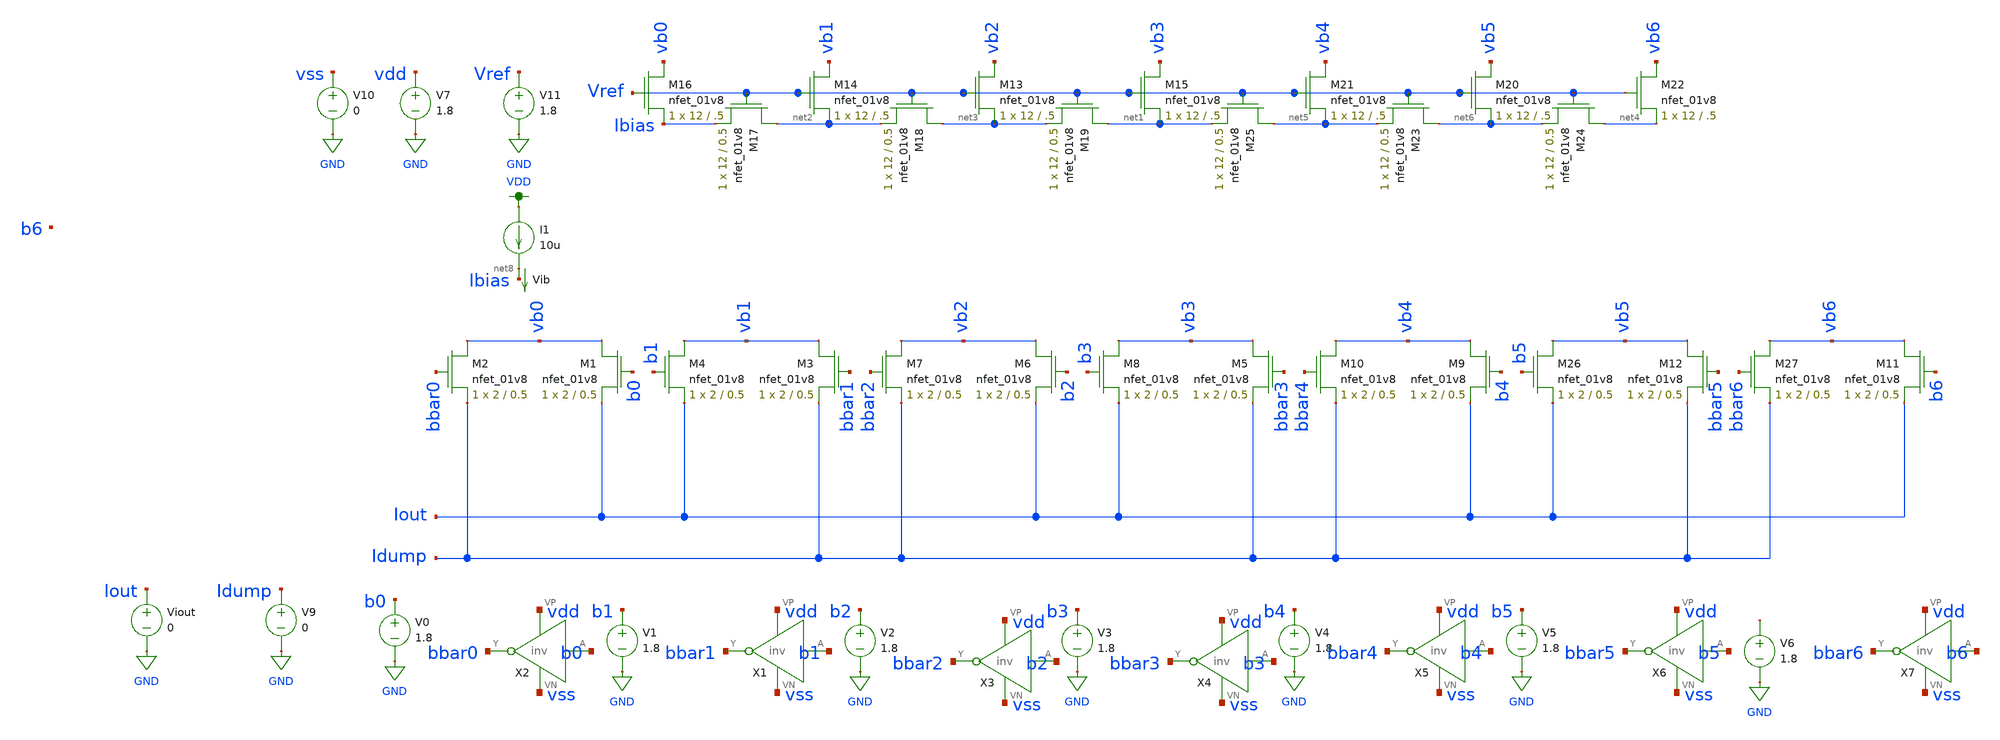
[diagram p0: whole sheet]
** sch_path: DAC_Final.sch
**.subckt DAC_Final
XM16 vb0 Vref Ibias GND sky130_fd_pr__nfet_01v8 L=.5 W=12 nf=1 ad='int((nf+1)/2) * W/nf * 0.29' as='int((nf+2)/2) * W/nf * 0.29'
+ pd='2*int((nf+1)/2) * (W/nf + 0.29)' ps='2*int((nf+2)/2) * (W/nf + 0.29)' nrd='0.29 / W' nrs='0.29 / W'
+ sa=0 sb=0 sd=0 mult=1 m=1
XM17 net2 Vref Ibias GND sky130_fd_pr__nfet_01v8 L=0.5 W=12 nf=1 ad='int((nf+1)/2) * W/nf * 0.29' as='int((nf+2)/2) * W/nf * 0.29'
+ pd='2*int((nf+1)/2) * (W/nf + 0.29)' ps='2*int((nf+2)/2) * (W/nf + 0.29)' nrd='0.29 / W' nrs='0.29 / W'
+ sa=0 sb=0 sd=0 mult=1 m=1
XM18 net3 Vref net2 GND sky130_fd_pr__nfet_01v8 L=0.5 W=12 nf=1 ad='int((nf+1)/2) * W/nf * 0.29' as='int((nf+2)/2) * W/nf * 0.29'
+ pd='2*int((nf+1)/2) * (W/nf + 0.29)' ps='2*int((nf+2)/2) * (W/nf + 0.29)' nrd='0.29 / W' nrs='0.29 / W'
+ sa=0 sb=0 sd=0 mult=1 m=1
XM19 net1 Vref net3 GND sky130_fd_pr__nfet_01v8 L=0.5 W=12 nf=1 ad='int((nf+1)/2) * W/nf * 0.29' as='int((nf+2)/2) * W/nf * 0.29'
+ pd='2*int((nf+1)/2) * (W/nf + 0.29)' ps='2*int((nf+2)/2) * (W/nf + 0.29)' nrd='0.29 / W' nrs='0.29 / W'
+ sa=0 sb=0 sd=0 mult=1 m=1
XM23 net6 Vref net5 GND sky130_fd_pr__nfet_01v8 L=0.5 W=12 nf=1 ad='int((nf+1)/2) * W/nf * 0.29' as='int((nf+2)/2) * W/nf * 0.29'
+ pd='2*int((nf+1)/2) * (W/nf + 0.29)' ps='2*int((nf+2)/2) * (W/nf + 0.29)' nrd='0.29 / W' nrs='0.29 / W'
+ sa=0 sb=0 sd=0 mult=1 m=1
XM24 net4 Vref net6 GND sky130_fd_pr__nfet_01v8 L=0.5 W=12 nf=1 ad='int((nf+1)/2) * W/nf * 0.29' as='int((nf+2)/2) * W/nf * 0.29'
+ pd='2*int((nf+1)/2) * (W/nf + 0.29)' ps='2*int((nf+2)/2) * (W/nf + 0.29)' nrd='0.29 / W' nrs='0.29 / W'
+ sa=0 sb=0 sd=0 mult=1 m=1
XM25 net5 Vref net1 GND sky130_fd_pr__nfet_01v8 L=0.5 W=12 nf=1 ad='int((nf+1)/2) * W/nf * 0.29' as='int((nf+2)/2) * W/nf * 0.29'
+ pd='2*int((nf+1)/2) * (W/nf + 0.29)' ps='2*int((nf+2)/2) * (W/nf + 0.29)' nrd='0.29 / W' nrs='0.29 / W'
+ sa=0 sb=0 sd=0 mult=1 m=1
V11 Vref GND 1.8
V0 b0 GND 1.8
V1 b1 GND 1.8
V2 b2 GND 1.8
V3 b3 GND 1.8
V4 b4 GND 1.8
V5 b5 GND 1.8
V6 net7 GND 1.8
XM14 vb1 Vref net2 GND sky130_fd_pr__nfet_01v8 L=.5 W=12 nf=1 ad='int((nf+1)/2) * W/nf * 0.29' as='int((nf+2)/2) * W/nf * 0.29'
+ pd='2*int((nf+1)/2) * (W/nf + 0.29)' ps='2*int((nf+2)/2) * (W/nf + 0.29)' nrd='0.29 / W' nrs='0.29 / W'
+ sa=0 sb=0 sd=0 mult=1 m=1
XM13 vb2 Vref net3 GND sky130_fd_pr__nfet_01v8 L=.5 W=12 nf=1 ad='int((nf+1)/2) * W/nf * 0.29' as='int((nf+2)/2) * W/nf * 0.29'
+ pd='2*int((nf+1)/2) * (W/nf + 0.29)' ps='2*int((nf+2)/2) * (W/nf + 0.29)' nrd='0.29 / W' nrs='0.29 / W'
+ sa=0 sb=0 sd=0 mult=1 m=1
XM15 vb3 Vref net1 GND sky130_fd_pr__nfet_01v8 L=.5 W=12 nf=1 ad='int((nf+1)/2) * W/nf * 0.29' as='int((nf+2)/2) * W/nf * 0.29'
+ pd='2*int((nf+1)/2) * (W/nf + 0.29)' ps='2*int((nf+2)/2) * (W/nf + 0.29)' nrd='0.29 / W' nrs='0.29 / W'
+ sa=0 sb=0 sd=0 mult=1 m=1
XM22 vb6 Vref net4 GND sky130_fd_pr__nfet_01v8 L=.5 W=12 nf=1 ad='int((nf+1)/2) * W/nf * 0.29' as='int((nf+2)/2) * W/nf * 0.29'
+ pd='2*int((nf+1)/2) * (W/nf + 0.29)' ps='2*int((nf+2)/2) * (W/nf + 0.29)' nrd='0.29 / W' nrs='0.29 / W'
+ sa=0 sb=0 sd=0 mult=1 m=1
XM20 vb5 Vref net6 GND sky130_fd_pr__nfet_01v8 L=.5 W=12 nf=1 ad='int((nf+1)/2) * W/nf * 0.29' as='int((nf+2)/2) * W/nf * 0.29'
+ pd='2*int((nf+1)/2) * (W/nf + 0.29)' ps='2*int((nf+2)/2) * (W/nf + 0.29)' nrd='0.29 / W' nrs='0.29 / W'
+ sa=0 sb=0 sd=0 mult=1 m=1
XM21 vb4 Vref net5 GND sky130_fd_pr__nfet_01v8 L=.5 W=12 nf=1 ad='int((nf+1)/2) * W/nf * 0.29' as='int((nf+2)/2) * W/nf * 0.29'
+ pd='2*int((nf+1)/2) * (W/nf + 0.29)' ps='2*int((nf+2)/2) * (W/nf + 0.29)' nrd='0.29 / W' nrs='0.29 / W'
+ sa=0 sb=0 sd=0 mult=1 m=1
V9 Idump GND 0
Viout Iout GND 0
XM1 vb0 b0 Iout GND sky130_fd_pr__nfet_01v8 L=0.5 W=2 nf=1 ad='int((nf+1)/2) * W/nf * 0.29' as='int((nf+2)/2) * W/nf * 0.29'
+ pd='2*int((nf+1)/2) * (W/nf + 0.29)' ps='2*int((nf+2)/2) * (W/nf + 0.29)' nrd='0.29 / W' nrs='0.29 / W'
+ sa=0 sb=0 sd=0 mult=1 m=1
XM2 vb0 bbar0 Idump GND sky130_fd_pr__nfet_01v8 L=0.5 W=2 nf=1 ad='int((nf+1)/2) * W/nf * 0.29' as='int((nf+2)/2) * W/nf * 0.29'
+ pd='2*int((nf+1)/2) * (W/nf + 0.29)' ps='2*int((nf+2)/2) * (W/nf + 0.29)' nrd='0.29 / W' nrs='0.29 / W'
+ sa=0 sb=0 sd=0 mult=1 m=1
XM3 vb1 bbar1 Idump GND sky130_fd_pr__nfet_01v8 L=0.5 W=2 nf=1 ad='int((nf+1)/2) * W/nf * 0.29' as='int((nf+2)/2) * W/nf * 0.29'
+ pd='2*int((nf+1)/2) * (W/nf + 0.29)' ps='2*int((nf+2)/2) * (W/nf + 0.29)' nrd='0.29 / W' nrs='0.29 / W'
+ sa=0 sb=0 sd=0 mult=1 m=1
XM4 vb1 b1 Iout GND sky130_fd_pr__nfet_01v8 L=0.5 W=2 nf=1 ad='int((nf+1)/2) * W/nf * 0.29' as='int((nf+2)/2) * W/nf * 0.29'
+ pd='2*int((nf+1)/2) * (W/nf + 0.29)' ps='2*int((nf+2)/2) * (W/nf + 0.29)' nrd='0.29 / W' nrs='0.29 / W'
+ sa=0 sb=0 sd=0 mult=1 m=1
XM6 vb2 b2 Iout GND sky130_fd_pr__nfet_01v8 L=0.5 W=2 nf=1 ad='int((nf+1)/2) * W/nf * 0.29' as='int((nf+2)/2) * W/nf * 0.29'
+ pd='2*int((nf+1)/2) * (W/nf + 0.29)' ps='2*int((nf+2)/2) * (W/nf + 0.29)' nrd='0.29 / W' nrs='0.29 / W'
+ sa=0 sb=0 sd=0 mult=1 m=1
XM7 vb2 bbar2 Idump GND sky130_fd_pr__nfet_01v8 L=0.5 W=2 nf=1 ad='int((nf+1)/2) * W/nf * 0.29' as='int((nf+2)/2) * W/nf * 0.29'
+ pd='2*int((nf+1)/2) * (W/nf + 0.29)' ps='2*int((nf+2)/2) * (W/nf + 0.29)' nrd='0.29 / W' nrs='0.29 / W'
+ sa=0 sb=0 sd=0 mult=1 m=1
XM5 vb3 bbar3 Idump GND sky130_fd_pr__nfet_01v8 L=0.5 W=2 nf=1 ad='int((nf+1)/2) * W/nf * 0.29' as='int((nf+2)/2) * W/nf * 0.29'
+ pd='2*int((nf+1)/2) * (W/nf + 0.29)' ps='2*int((nf+2)/2) * (W/nf + 0.29)' nrd='0.29 / W' nrs='0.29 / W'
+ sa=0 sb=0 sd=0 mult=1 m=1
XM8 vb3 b3 Iout GND sky130_fd_pr__nfet_01v8 L=0.5 W=2 nf=1 ad='int((nf+1)/2) * W/nf * 0.29' as='int((nf+2)/2) * W/nf * 0.29'
+ pd='2*int((nf+1)/2) * (W/nf + 0.29)' ps='2*int((nf+2)/2) * (W/nf + 0.29)' nrd='0.29 / W' nrs='0.29 / W'
+ sa=0 sb=0 sd=0 mult=1 m=1
XM9 vb4 b4 Iout GND sky130_fd_pr__nfet_01v8 L=0.5 W=2 nf=1 ad='int((nf+1)/2) * W/nf * 0.29' as='int((nf+2)/2) * W/nf * 0.29'
+ pd='2*int((nf+1)/2) * (W/nf + 0.29)' ps='2*int((nf+2)/2) * (W/nf + 0.29)' nrd='0.29 / W' nrs='0.29 / W'
+ sa=0 sb=0 sd=0 mult=1 m=1
XM10 vb4 bbar4 Idump GND sky130_fd_pr__nfet_01v8 L=0.5 W=2 nf=1 ad='int((nf+1)/2) * W/nf * 0.29' as='int((nf+2)/2) * W/nf * 0.29'
+ pd='2*int((nf+1)/2) * (W/nf + 0.29)' ps='2*int((nf+2)/2) * (W/nf + 0.29)' nrd='0.29 / W' nrs='0.29 / W'
+ sa=0 sb=0 sd=0 mult=1 m=1
XM12 vb5 bbar5 Idump GND sky130_fd_pr__nfet_01v8 L=0.5 W=2 nf=1 ad='int((nf+1)/2) * W/nf * 0.29' as='int((nf+2)/2) * W/nf * 0.29'
+ pd='2*int((nf+1)/2) * (W/nf + 0.29)' ps='2*int((nf+2)/2) * (W/nf + 0.29)' nrd='0.29 / W' nrs='0.29 / W'
+ sa=0 sb=0 sd=0 mult=1 m=1
XM26 vb5 b5 Iout GND sky130_fd_pr__nfet_01v8 L=0.5 W=2 nf=1 ad='int((nf+1)/2) * W/nf * 0.29' as='int((nf+2)/2) * W/nf * 0.29'
+ pd='2*int((nf+1)/2) * (W/nf + 0.29)' ps='2*int((nf+2)/2) * (W/nf + 0.29)' nrd='0.29 / W' nrs='0.29 / W'
+ sa=0 sb=0 sd=0 mult=1 m=1
XM11 vb6 b6 Iout GND sky130_fd_pr__nfet_01v8 L=0.5 W=2 nf=1 ad='int((nf+1)/2) * W/nf * 0.29' as='int((nf+2)/2) * W/nf * 0.29'
+ pd='2*int((nf+1)/2) * (W/nf + 0.29)' ps='2*int((nf+2)/2) * (W/nf + 0.29)' nrd='0.29 / W' nrs='0.29 / W'
+ sa=0 sb=0 sd=0 mult=1 m=1
XM27 vb6 bbar6 Idump GND sky130_fd_pr__nfet_01v8 L=0.5 W=2 nf=1 ad='int((nf+1)/2) * W/nf * 0.29' as='int((nf+2)/2) * W/nf * 0.29'
+ pd='2*int((nf+1)/2) * (W/nf + 0.29)' ps='2*int((nf+2)/2) * (W/nf + 0.29)' nrd='0.29 / W' nrs='0.29 / W'
+ sa=0 sb=0 sd=0 mult=1 m=1
V7 vdd GND 1.8
V10 vss GND 0
X2 b0 bbar0 vdd vss inv
X1 b1 bbar1 vdd vss inv
X3 b2 bbar2 vdd vss inv
X4 b3 bbar3 vdd vss inv
X5 b4 bbar4 vdd vss inv
X6 b5 bbar5 vdd vss inv
X7 b6 bbar6 vdd vss inv
I1 VDD net8 10u
Vib net8 Ibias 0
.save i(vib)
**** begin user architecture code

.option wnflag=1
.param MC_SWITCH=1.0
.lib /usr/local/share/pdk/sky130A/libs.tech/ngspice/sky130.lib.spice tt


.save all
.control
set wr_vecnames
set wr_singlescale

let Ibias_max = 31n
let Ibias = 30n
dowhile Ibias < Ibias_max
alter Ib $&Ibias

let mc_runs = 1
let run = 1
dowhile run <= mc_runs

  let code = 0
  while code < 128
    if floor(code / 1) eq 0
      let b0 = 0
    else
      let b0 = (floor(code / 1) % 2) * 1.8
    end
    if floor(code / 2) eq 0
      let b1 = 0
    else
      let b1 = (floor(code / 2) % 2) * 1.8
    end
    if floor(code / 4) eq 0
      let b2 = 0
    else
      let b2 = (floor(code / 4) % 2) * 1.8
    end
    if floor(code / 8) eq 0
      let b3 = 0
    else
      let b3 = (floor(code / 8) % 2) * 1.8
    end
    if floor(code / 16) eq 0
      let b4 = 0
    else
      let b4 = (floor(code / 16) % 2) * 1.8
    end
    if floor(code / 32) eq 0
      let b5 = 0
    else
      let b5 = (floor(code / 32) % 2) * 1.8
    end
    if floor(code / 64) eq 0
      let b6 = 0
    else
      let b6 = (floor(code / 64) % 2) * 1.8
    end

    alter V0 $&b0
    alter V1 $&b1
    alter V2 $&b2
    alter V3 $&b3
    alter V4 $&b4
    alter V5 $&b5
    alter V6 $&b6
    save all
    op

    wrdata /home/madvlsi/madvlsi/mp3/DACOutput_{$&run}.txt v(b0) v(b1) v(b2) v(b3) v(b4) v(b5) v(b6)
+ i(Vib) i(Viout)
    if code eq 0
      set appendwrite
      set wr_vecnames = FALSE
    end
    let code = code + 1
  end
  reset
  set appendwrite = FALSE
  set wr_vecnames
  let run = run + 1
end

let Ibias = Ibias * 2
end
.endc

**** end user architecture code
**.ends

* expanding   symbol:  /home/madvlsi/madvlsi/mp1/xschem/inv.sym # of pins=4
** sym_path: MP2/inv.sym
** sch_path: MP2/inv.sch
.subckt inv A Y VP VN
*.ipin A
*.opin Y
*.iopin VN
*.iopin VP
XM3 Y A VP VP sky130_fd_pr__pfet_01v8 L=0.15 W=1 nf=1 ad='int((nf+1)/2) * W/nf * 0.29' as='int((nf+2)/2) * W/nf * 0.29'
+ pd='2*int((nf+1)/2) * (W/nf + 0.29)' ps='2*int((nf+2)/2) * (W/nf + 0.29)' nrd='0.29 / W' nrs='0.29 / W'
+ sa=0 sb=0 sd=0 mult=1 m=1
XM1 Y A VN VN sky130_fd_pr__nfet_01v8 L=0.15 W=1 nf=1 ad='int((nf+1)/2) * W/nf * 0.29' as='int((nf+2)/2) * W/nf * 0.29'
+ pd='2*int((nf+1)/2) * (W/nf + 0.29)' ps='2*int((nf+2)/2) * (W/nf + 0.29)' nrd='0.29 / W' nrs='0.29 / W'
+ sa=0 sb=0 sd=0 mult=1 m=1
**** begin user architecture code





**** end user architecture code
.ends

.GLOBAL GND
.GLOBAL VDD
.end
